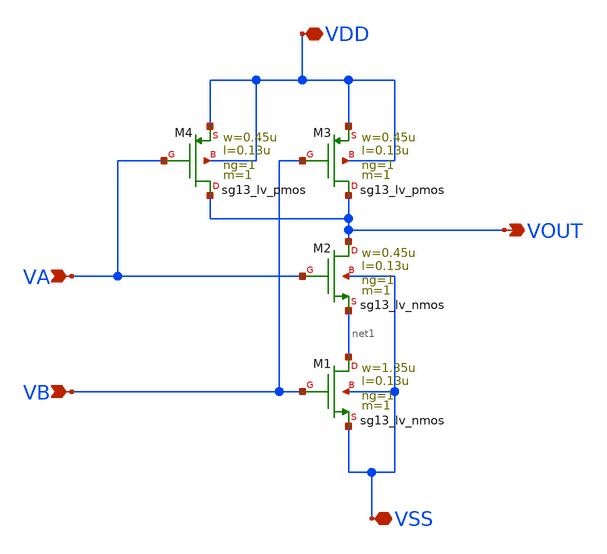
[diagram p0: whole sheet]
** sch_path: ADC8711-main/schematic/xschem/NAND_D3.sch
**.subckt NAND_D3 VDD VSS VA VB VOUT
*.iopin VDD
*.iopin VSS
*.ipin VA
*.ipin VB
*.opin VOUT
XM1 net1 VB VSS VSS sg13_lv_nmos w=1.35u l=0.13u ng=1 m=1 mm_ok=1
XM2 VOUT VA net1 VSS sg13_lv_nmos w=0.45u l=0.13u ng=1 m=1 mm_ok=1
XM3 VOUT VB VDD VDD sg13_lv_pmos w=0.45u l=0.13u ng=1 m=1 mm_ok=1
XM4 VOUT VA VDD VDD sg13_lv_pmos w=0.45u l=0.13u ng=1 m=1 mm_ok=1
**.ends
.end
